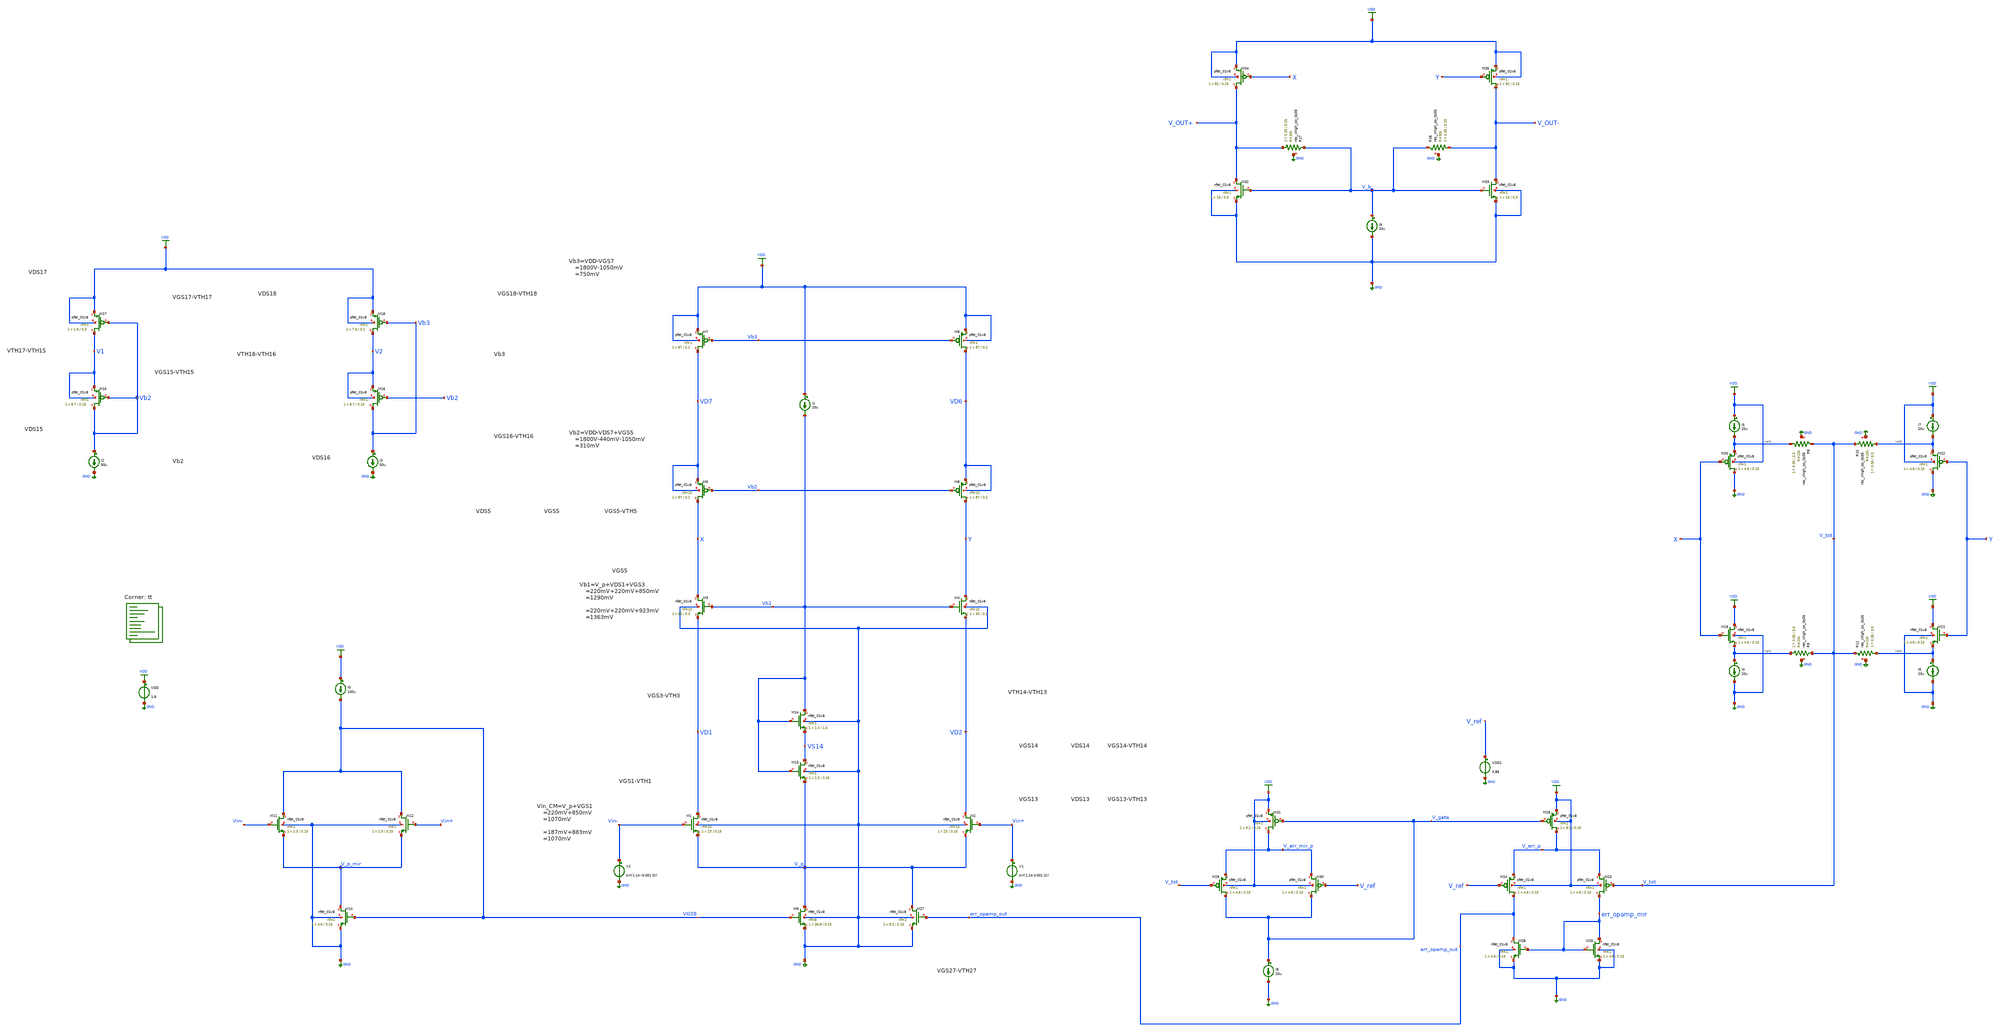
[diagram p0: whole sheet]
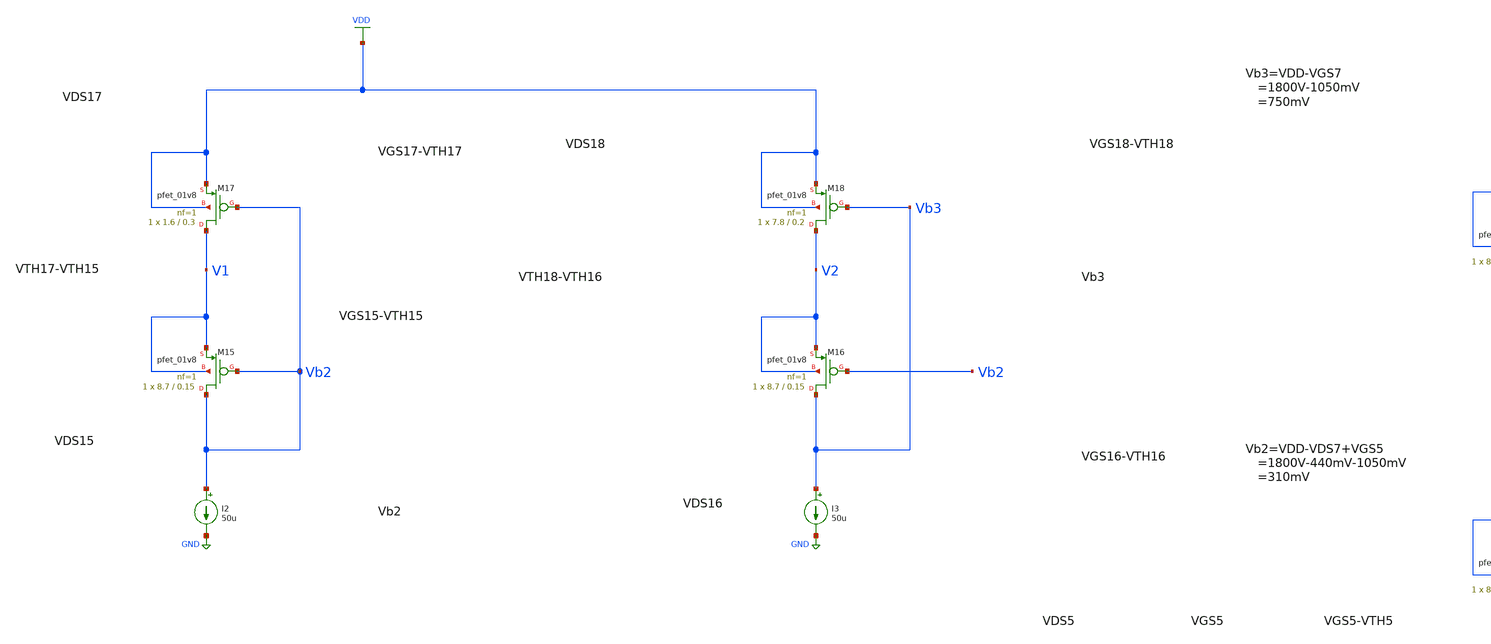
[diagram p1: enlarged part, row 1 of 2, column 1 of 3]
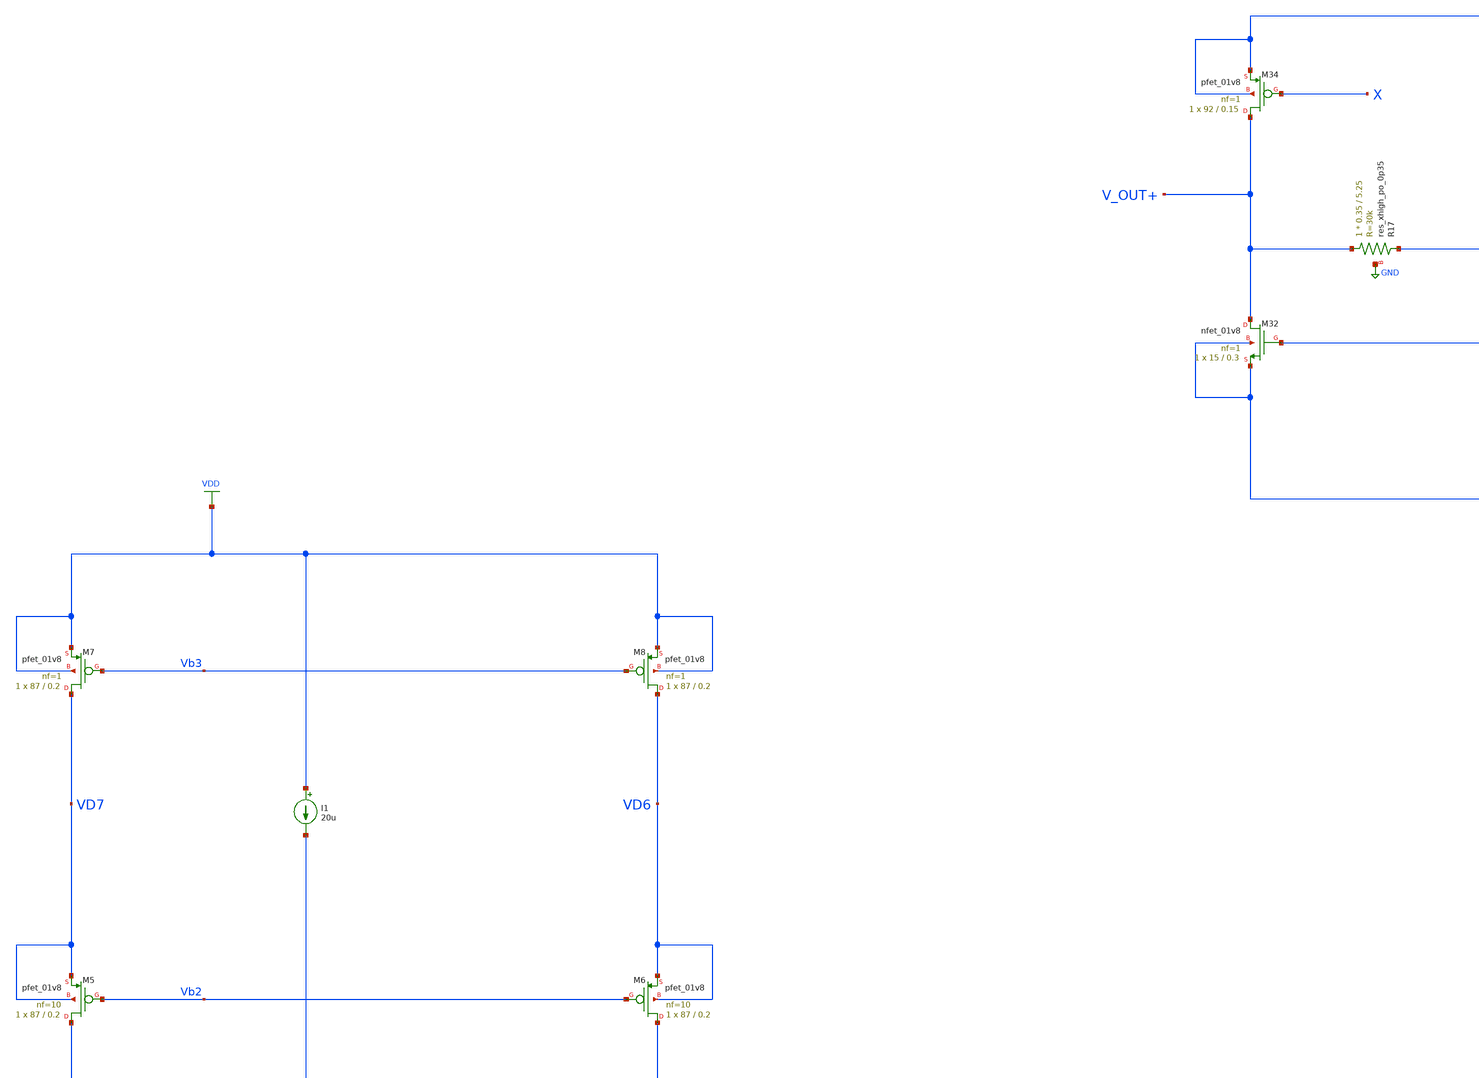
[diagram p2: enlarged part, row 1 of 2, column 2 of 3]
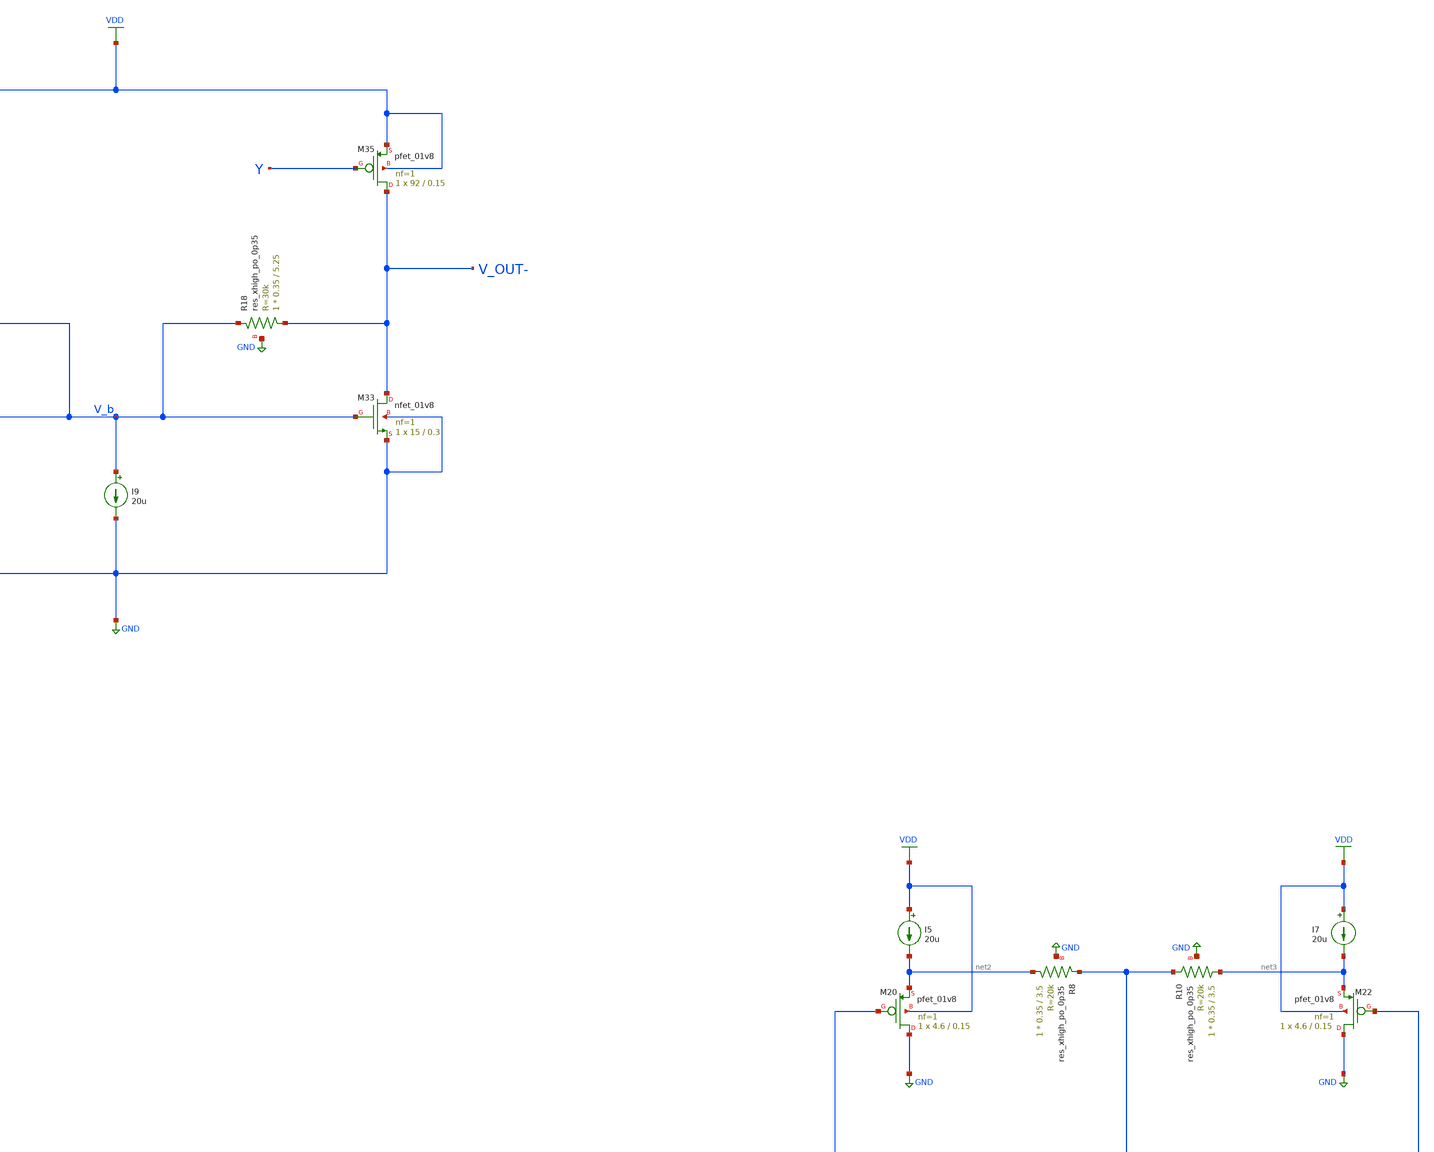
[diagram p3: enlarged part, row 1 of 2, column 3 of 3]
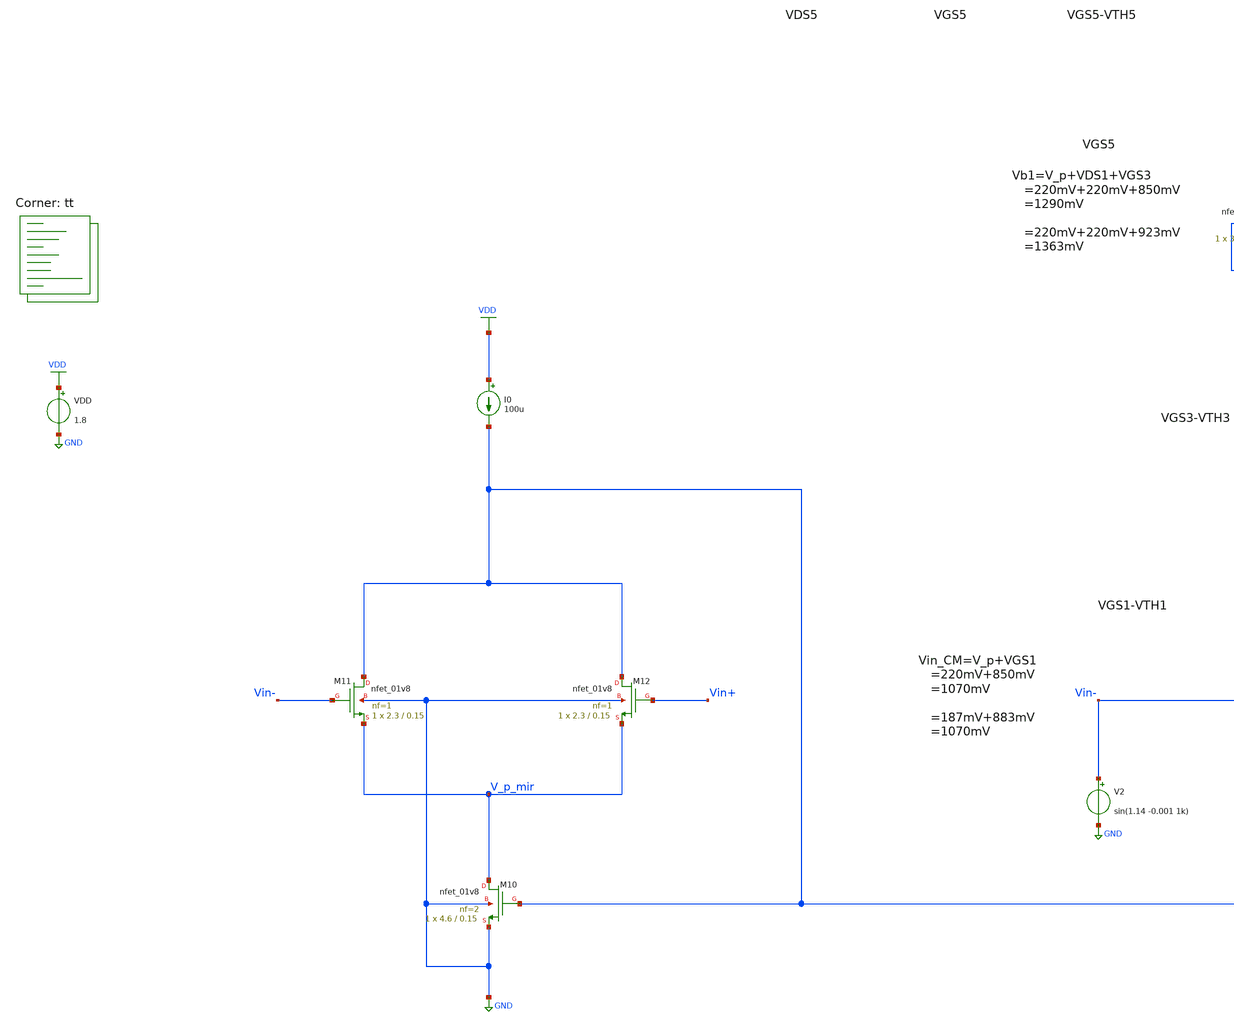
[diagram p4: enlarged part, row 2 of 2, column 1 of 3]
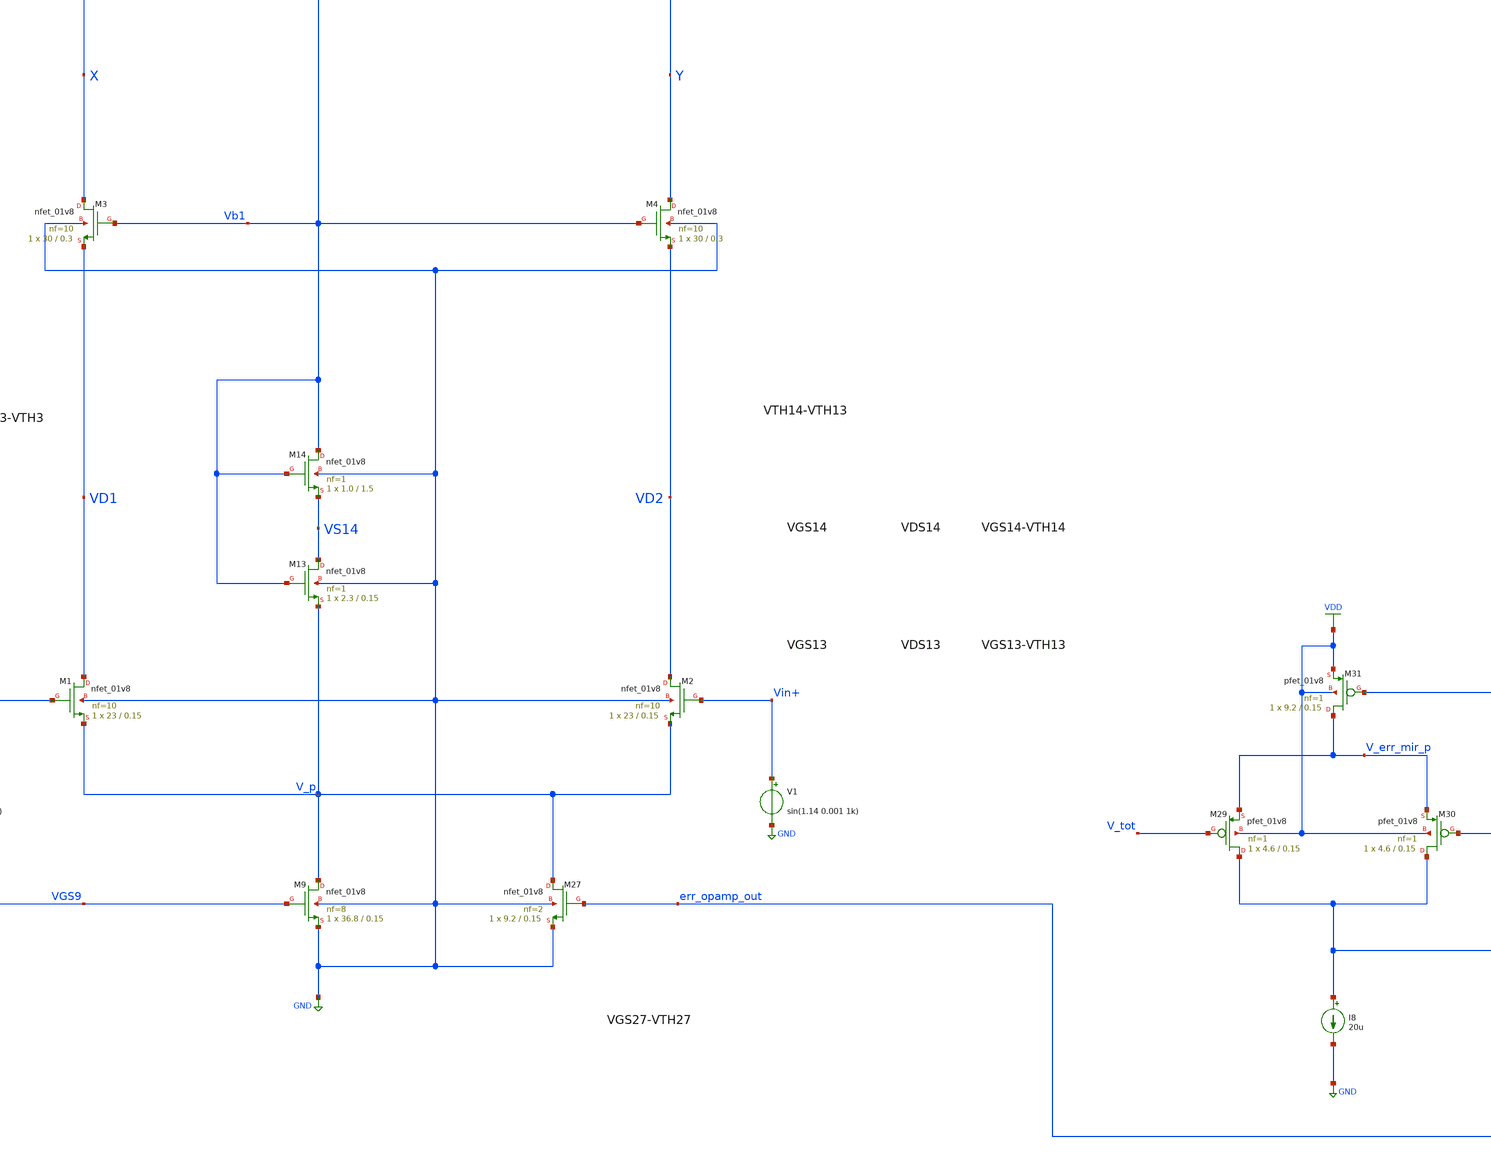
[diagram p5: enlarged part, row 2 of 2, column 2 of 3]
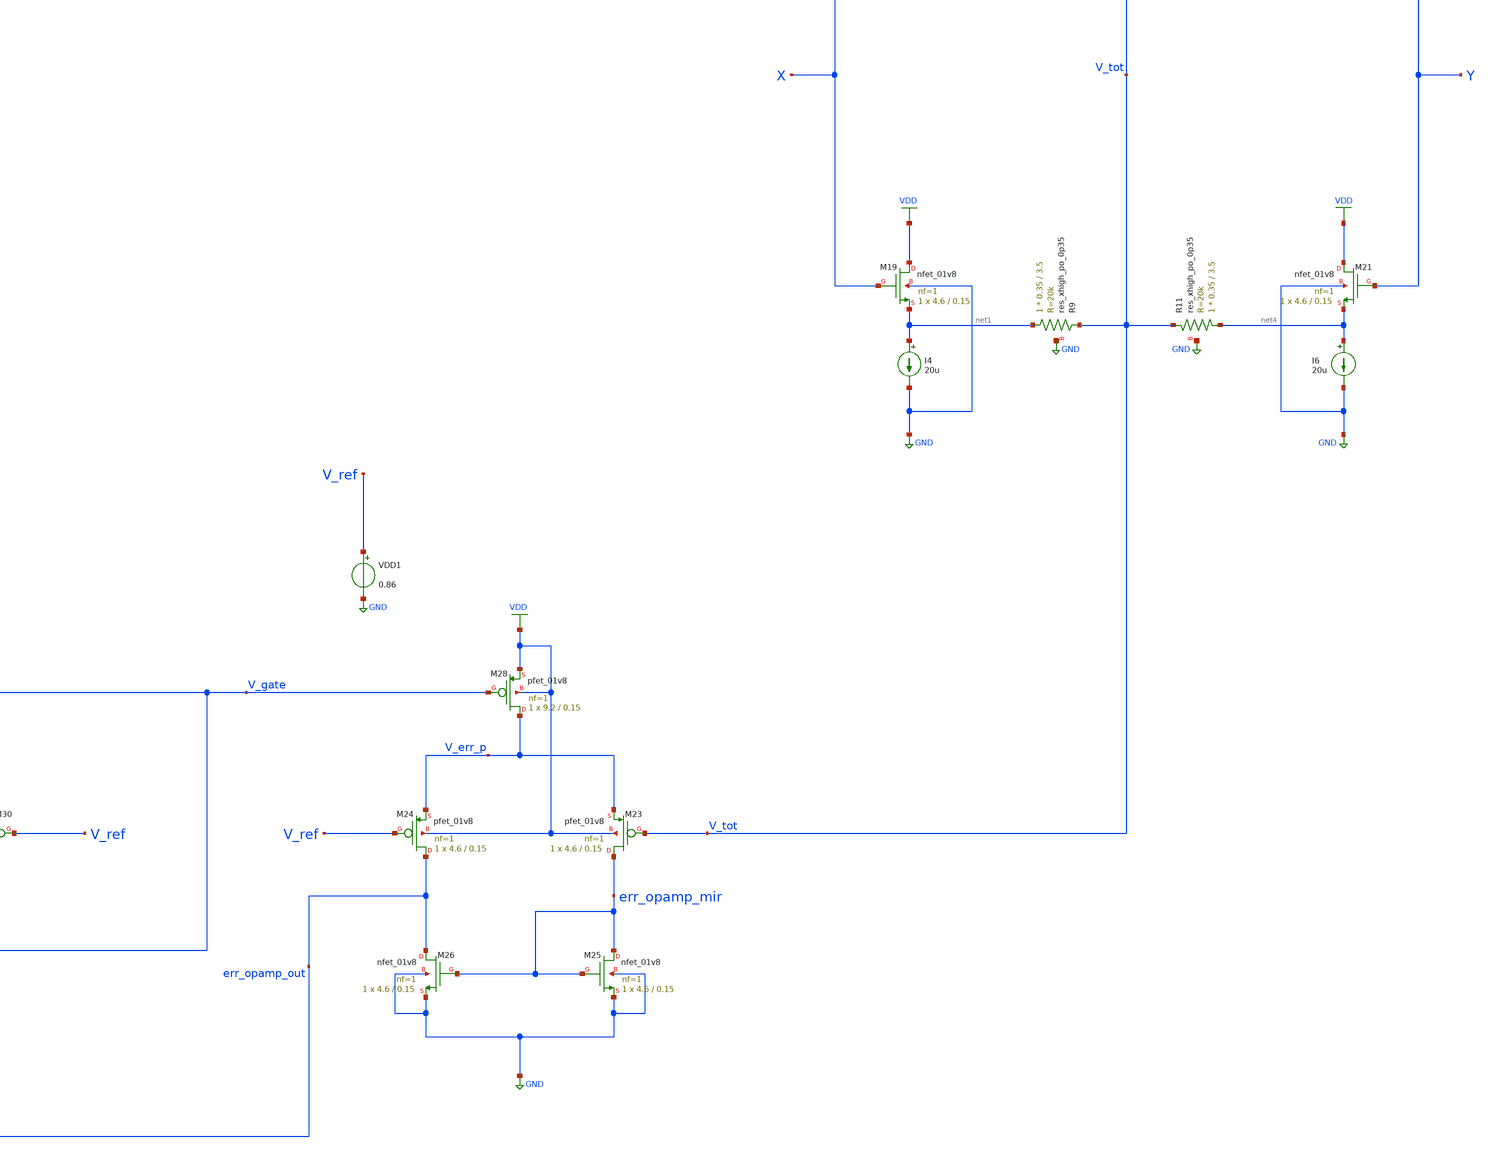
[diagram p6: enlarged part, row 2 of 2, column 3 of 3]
** sch_path: projects/opamp/xschem_ngspice/opamp_1st_stage_bias_check.sch
**.subckt opamp_1st_stage_bias_check
VDD VDD GND 1.8
XM1 VD1 Vin- V_p GND sky130_fd_pr__nfet_01v8 L=0.15 W=23 nf=10 ad='int((nf+1)/2) * W/nf * 0.29' as='int((nf+2)/2) * W/nf * 0.29'
+ pd='2*int((nf+1)/2) * (W/nf + 0.29)' ps='2*int((nf+2)/2) * (W/nf + 0.29)' nrd='0.29 / W' nrs='0.29 / W'
+ sa=0 sb=0 sd=0 mult=1 m=1
XM2 VD2 Vin+ V_p GND sky130_fd_pr__nfet_01v8 L=0.15 W=23 nf=10 ad='int((nf+1)/2) * W/nf * 0.29' as='int((nf+2)/2) * W/nf * 0.29'
+ pd='2*int((nf+1)/2) * (W/nf + 0.29)' ps='2*int((nf+2)/2) * (W/nf + 0.29)' nrd='0.29 / W' nrs='0.29 / W'
+ sa=0 sb=0 sd=0 mult=1 m=1
XM3 X Vb1 VD1 GND sky130_fd_pr__nfet_01v8 L=0.3 W=30 nf=10 ad='int((nf+1)/2) * W/nf * 0.29' as='int((nf+2)/2) * W/nf * 0.29'
+ pd='2*int((nf+1)/2) * (W/nf + 0.29)' ps='2*int((nf+2)/2) * (W/nf + 0.29)' nrd='0.29 / W' nrs='0.29 / W'
+ sa=0 sb=0 sd=0 mult=1 m=1
XM4 Y Vb1 VD2 GND sky130_fd_pr__nfet_01v8 L=0.3 W=30 nf=10 ad='int((nf+1)/2) * W/nf * 0.29' as='int((nf+2)/2) * W/nf * 0.29'
+ pd='2*int((nf+1)/2) * (W/nf + 0.29)' ps='2*int((nf+2)/2) * (W/nf + 0.29)' nrd='0.29 / W' nrs='0.29 / W'
+ sa=0 sb=0 sd=0 mult=1 m=1
XM5 X Vb2 VD7 VD7 sky130_fd_pr__pfet_01v8 L=0.2 W=87 nf=10 ad='int((nf+1)/2) * W/nf * 0.29' as='int((nf+2)/2) * W/nf * 0.29'
+ pd='2*int((nf+1)/2) * (W/nf + 0.29)' ps='2*int((nf+2)/2) * (W/nf + 0.29)' nrd='0.29 / W' nrs='0.29 / W'
+ sa=0 sb=0 sd=0 mult=1 m=1
XM6 Y Vb2 VD6 VD6 sky130_fd_pr__pfet_01v8 L=0.2 W=87 nf=10 ad='int((nf+1)/2) * W/nf * 0.29' as='int((nf+2)/2) * W/nf * 0.29'
+ pd='2*int((nf+1)/2) * (W/nf + 0.29)' ps='2*int((nf+2)/2) * (W/nf + 0.29)' nrd='0.29 / W' nrs='0.29 / W'
+ sa=0 sb=0 sd=0 mult=1 m=1
XM7 VD7 Vb3 VDD VDD sky130_fd_pr__pfet_01v8 L=0.2 W=87 nf=1 ad='int((nf+1)/2) * W/nf * 0.29' as='int((nf+2)/2) * W/nf * 0.29'
+ pd='2*int((nf+1)/2) * (W/nf + 0.29)' ps='2*int((nf+2)/2) * (W/nf + 0.29)' nrd='0.29 / W' nrs='0.29 / W'
+ sa=0 sb=0 sd=0 mult=1 m=1
XM8 VD6 Vb3 VDD VDD sky130_fd_pr__pfet_01v8 L=0.2 W=87 nf=1 ad='int((nf+1)/2) * W/nf * 0.29' as='int((nf+2)/2) * W/nf * 0.29'
+ pd='2*int((nf+1)/2) * (W/nf + 0.29)' ps='2*int((nf+2)/2) * (W/nf + 0.29)' nrd='0.29 / W' nrs='0.29 / W'
+ sa=0 sb=0 sd=0 mult=1 m=1
XM9 V_p VGS9 GND GND sky130_fd_pr__nfet_01v8 L=0.15 W=36.8 nf=8 ad='int((nf+1)/2) * W/nf * 0.29' as='int((nf+2)/2) * W/nf * 0.29'
+ pd='2*int((nf+1)/2) * (W/nf + 0.29)' ps='2*int((nf+2)/2) * (W/nf + 0.29)' nrd='0.29 / W' nrs='0.29 / W'
+ sa=0 sb=0 sd=0 mult=1 m=1
V1 Vin+ GND sin(1.14 0.001 1k)
XM10 V_p_mir VGS9 GND GND sky130_fd_pr__nfet_01v8 L=0.15 W=4.6 nf=2 ad='int((nf+1)/2) * W/nf * 0.29'
+ as='int((nf+2)/2) * W/nf * 0.29' pd='2*int((nf+1)/2) * (W/nf + 0.29)' ps='2*int((nf+2)/2) * (W/nf + 0.29)'
+ nrd='0.29 / W' nrs='0.29 / W' sa=0 sb=0 sd=0 mult=1 m=1
I0 VDD VGS9 100u
XM11 VGS9 Vin- V_p_mir GND sky130_fd_pr__nfet_01v8 L=0.15 W=2.3 nf=1 ad='int((nf+1)/2) * W/nf * 0.29'
+ as='int((nf+2)/2) * W/nf * 0.29' pd='2*int((nf+1)/2) * (W/nf + 0.29)' ps='2*int((nf+2)/2) * (W/nf + 0.29)'
+ nrd='0.29 / W' nrs='0.29 / W' sa=0 sb=0 sd=0 mult=1 m=1
XM12 VGS9 Vin+ V_p_mir GND sky130_fd_pr__nfet_01v8 L=0.15 W=2.3 nf=1 ad='int((nf+1)/2) * W/nf * 0.29'
+ as='int((nf+2)/2) * W/nf * 0.29' pd='2*int((nf+1)/2) * (W/nf + 0.29)' ps='2*int((nf+2)/2) * (W/nf + 0.29)'
+ nrd='0.29 / W' nrs='0.29 / W' sa=0 sb=0 sd=0 mult=1 m=1
XM13 VS14 Vb1 V_p GND sky130_fd_pr__nfet_01v8 L=0.15 W=2.3 nf=1 ad='int((nf+1)/2) * W/nf * 0.29' as='int((nf+2)/2) * W/nf * 0.29'
+ pd='2*int((nf+1)/2) * (W/nf + 0.29)' ps='2*int((nf+2)/2) * (W/nf + 0.29)' nrd='0.29 / W' nrs='0.29 / W'
+ sa=0 sb=0 sd=0 mult=1 m=1
XM14 Vb1 Vb1 VS14 GND sky130_fd_pr__nfet_01v8 L=1.5 W=1.0 nf=1 ad='int((nf+1)/2) * W/nf * 0.29' as='int((nf+2)/2) * W/nf * 0.29'
+ pd='2*int((nf+1)/2) * (W/nf + 0.29)' ps='2*int((nf+2)/2) * (W/nf + 0.29)' nrd='0.29 / W' nrs='0.29 / W'
+ sa=0 sb=0 sd=0 mult=1 m=1
I1 VDD Vb1 20u
XM15 Vb2 Vb2 V1 V1 sky130_fd_pr__pfet_01v8 L=0.15 W=8.7 nf=1 ad='int((nf+1)/2) * W/nf * 0.29' as='int((nf+2)/2) * W/nf * 0.29'
+ pd='2*int((nf+1)/2) * (W/nf + 0.29)' ps='2*int((nf+2)/2) * (W/nf + 0.29)' nrd='0.29 / W' nrs='0.29 / W'
+ sa=0 sb=0 sd=0 mult=1 m=1
XM16 Vb3 Vb2 V2 V2 sky130_fd_pr__pfet_01v8 L=0.15 W=8.7 nf=1 ad='int((nf+1)/2) * W/nf * 0.29' as='int((nf+2)/2) * W/nf * 0.29'
+ pd='2*int((nf+1)/2) * (W/nf + 0.29)' ps='2*int((nf+2)/2) * (W/nf + 0.29)' nrd='0.29 / W' nrs='0.29 / W'
+ sa=0 sb=0 sd=0 mult=1 m=1
XM17 V1 Vb2 VDD VDD sky130_fd_pr__pfet_01v8 L=0.3 W=1.6 nf=1 ad='int((nf+1)/2) * W/nf * 0.29' as='int((nf+2)/2) * W/nf * 0.29'
+ pd='2*int((nf+1)/2) * (W/nf + 0.29)' ps='2*int((nf+2)/2) * (W/nf + 0.29)' nrd='0.29 / W' nrs='0.29 / W'
+ sa=0 sb=0 sd=0 mult=1 m=1
XM18 V2 Vb3 VDD VDD sky130_fd_pr__pfet_01v8 L=0.2 W=7.8 nf=1 ad='int((nf+1)/2) * W/nf * 0.29' as='int((nf+2)/2) * W/nf * 0.29'
+ pd='2*int((nf+1)/2) * (W/nf + 0.29)' ps='2*int((nf+2)/2) * (W/nf + 0.29)' nrd='0.29 / W' nrs='0.29 / W'
+ sa=0 sb=0 sd=0 mult=1 m=1
I2 Vb2 GND 50u
I3 Vb3 GND 50u
XM19 VDD X net1 GND sky130_fd_pr__nfet_01v8 L=0.15 W=4.6 nf=1 ad='int((nf+1)/2) * W/nf * 0.29' as='int((nf+2)/2) * W/nf * 0.29'
+ pd='2*int((nf+1)/2) * (W/nf + 0.29)' ps='2*int((nf+2)/2) * (W/nf + 0.29)' nrd='0.29 / W' nrs='0.29 / W'
+ sa=0 sb=0 sd=0 mult=1 m=1
XM20 GND X net2 VDD sky130_fd_pr__pfet_01v8 L=0.15 W=4.6 nf=1 ad='int((nf+1)/2) * W/nf * 0.29' as='int((nf+2)/2) * W/nf * 0.29'
+ pd='2*int((nf+1)/2) * (W/nf + 0.29)' ps='2*int((nf+2)/2) * (W/nf + 0.29)' nrd='0.29 / W' nrs='0.29 / W'
+ sa=0 sb=0 sd=0 mult=1 m=1
I4 net1 GND 20u
I5 VDD net2 20u
XR8 net2 V_tot GND sky130_fd_pr__res_xhigh_po_0p35 L=3.5 mult=1 m=1
XR9 net1 V_tot GND sky130_fd_pr__res_xhigh_po_0p35 L=3.5 mult=1 m=1
XR10 net3 V_tot GND sky130_fd_pr__res_xhigh_po_0p35 L=3.5 mult=1 m=1
XR11 net4 V_tot GND sky130_fd_pr__res_xhigh_po_0p35 L=3.5 mult=1 m=1
XM21 VDD Y net4 GND sky130_fd_pr__nfet_01v8 L=0.15 W=4.6 nf=1 ad='int((nf+1)/2) * W/nf * 0.29' as='int((nf+2)/2) * W/nf * 0.29'
+ pd='2*int((nf+1)/2) * (W/nf + 0.29)' ps='2*int((nf+2)/2) * (W/nf + 0.29)' nrd='0.29 / W' nrs='0.29 / W'
+ sa=0 sb=0 sd=0 mult=1 m=1
XM22 GND Y net3 VDD sky130_fd_pr__pfet_01v8 L=0.15 W=4.6 nf=1 ad='int((nf+1)/2) * W/nf * 0.29' as='int((nf+2)/2) * W/nf * 0.29'
+ pd='2*int((nf+1)/2) * (W/nf + 0.29)' ps='2*int((nf+2)/2) * (W/nf + 0.29)' nrd='0.29 / W' nrs='0.29 / W'
+ sa=0 sb=0 sd=0 mult=1 m=1
I6 net4 GND 20u
I7 VDD net3 20u
XM23 err_opamp_mir V_tot V_err_p VDD sky130_fd_pr__pfet_01v8 L=0.15 W=4.6 nf=1 ad='int((nf+1)/2) * W/nf * 0.29'
+ as='int((nf+2)/2) * W/nf * 0.29' pd='2*int((nf+1)/2) * (W/nf + 0.29)' ps='2*int((nf+2)/2) * (W/nf + 0.29)'
+ nrd='0.29 / W' nrs='0.29 / W' sa=0 sb=0 sd=0 mult=1 m=1
XM24 err_opamp_out V_ref V_err_p VDD sky130_fd_pr__pfet_01v8 L=0.15 W=4.6 nf=1 ad='int((nf+1)/2) * W/nf * 0.29'
+ as='int((nf+2)/2) * W/nf * 0.29' pd='2*int((nf+1)/2) * (W/nf + 0.29)' ps='2*int((nf+2)/2) * (W/nf + 0.29)'
+ nrd='0.29 / W' nrs='0.29 / W' sa=0 sb=0 sd=0 mult=1 m=1
I8 V_gate GND 20u
XM25 err_opamp_mir err_opamp_mir GND GND sky130_fd_pr__nfet_01v8 L=0.15 W=4.6 nf=1 ad='int((nf+1)/2) * W/nf * 0.29'
+ as='int((nf+2)/2) * W/nf * 0.29' pd='2*int((nf+1)/2) * (W/nf + 0.29)' ps='2*int((nf+2)/2) * (W/nf + 0.29)'
+ nrd='0.29 / W' nrs='0.29 / W' sa=0 sb=0 sd=0 mult=1 m=1
XM26 err_opamp_out err_opamp_mir GND GND sky130_fd_pr__nfet_01v8 L=0.15 W=4.6 nf=1 ad='int((nf+1)/2) * W/nf * 0.29'
+ as='int((nf+2)/2) * W/nf * 0.29' pd='2*int((nf+1)/2) * (W/nf + 0.29)' ps='2*int((nf+2)/2) * (W/nf + 0.29)'
+ nrd='0.29 / W' nrs='0.29 / W' sa=0 sb=0 sd=0 mult=1 m=1
XM27 V_p err_opamp_out GND GND sky130_fd_pr__nfet_01v8 L=0.15 W=9.2 nf=2 ad='int((nf+1)/2) * W/nf * 0.29'
+ as='int((nf+2)/2) * W/nf * 0.29' pd='2*int((nf+1)/2) * (W/nf + 0.29)' ps='2*int((nf+2)/2) * (W/nf + 0.29)'
+ nrd='0.29 / W' nrs='0.29 / W' sa=0 sb=0 sd=0 mult=1 m=1
VDD1 V_ref GND 0.86
XM28 V_err_p V_gate VDD VDD sky130_fd_pr__pfet_01v8 L=0.15 W=9.2 nf=1 ad='int((nf+1)/2) * W/nf * 0.29'
+ as='int((nf+2)/2) * W/nf * 0.29' pd='2*int((nf+1)/2) * (W/nf + 0.29)' ps='2*int((nf+2)/2) * (W/nf + 0.29)'
+ nrd='0.29 / W' nrs='0.29 / W' sa=0 sb=0 sd=0 mult=1 m=1
XM29 V_gate V_tot V_err_mir_p VDD sky130_fd_pr__pfet_01v8 L=0.15 W=4.6 nf=1 ad='int((nf+1)/2) * W/nf * 0.29'
+ as='int((nf+2)/2) * W/nf * 0.29' pd='2*int((nf+1)/2) * (W/nf + 0.29)' ps='2*int((nf+2)/2) * (W/nf + 0.29)'
+ nrd='0.29 / W' nrs='0.29 / W' sa=0 sb=0 sd=0 mult=1 m=1
XM30 V_gate V_ref V_err_mir_p VDD sky130_fd_pr__pfet_01v8 L=0.15 W=4.6 nf=1 ad='int((nf+1)/2) * W/nf * 0.29'
+ as='int((nf+2)/2) * W/nf * 0.29' pd='2*int((nf+1)/2) * (W/nf + 0.29)' ps='2*int((nf+2)/2) * (W/nf + 0.29)'
+ nrd='0.29 / W' nrs='0.29 / W' sa=0 sb=0 sd=0 mult=1 m=1
XM31 V_err_mir_p V_gate VDD VDD sky130_fd_pr__pfet_01v8 L=0.15 W=9.2 nf=1 ad='int((nf+1)/2) * W/nf * 0.29'
+ as='int((nf+2)/2) * W/nf * 0.29' pd='2*int((nf+1)/2) * (W/nf + 0.29)' ps='2*int((nf+2)/2) * (W/nf + 0.29)'
+ nrd='0.29 / W' nrs='0.29 / W' sa=0 sb=0 sd=0 mult=1 m=1
XM32 V_OUT+ V_b GND GND sky130_fd_pr__nfet_01v8 L=0.3 W=15 nf=1 ad='int((nf+1)/2) * W/nf * 0.29' as='int((nf+2)/2) * W/nf * 0.29'
+ pd='2*int((nf+1)/2) * (W/nf + 0.29)' ps='2*int((nf+2)/2) * (W/nf + 0.29)' nrd='0.29 / W' nrs='0.29 / W'
+ sa=0 sb=0 sd=0 mult=1 m=1
XM33 V_OUT- V_b GND GND sky130_fd_pr__nfet_01v8 L=0.3 W=15 nf=1 ad='int((nf+1)/2) * W/nf * 0.29' as='int((nf+2)/2) * W/nf * 0.29'
+ pd='2*int((nf+1)/2) * (W/nf + 0.29)' ps='2*int((nf+2)/2) * (W/nf + 0.29)' nrd='0.29 / W' nrs='0.29 / W'
+ sa=0 sb=0 sd=0 mult=1 m=1
XM34 V_OUT+ X VDD VDD sky130_fd_pr__pfet_01v8 L=0.15 W=92 nf=1 ad='int((nf+1)/2) * W/nf * 0.29' as='int((nf+2)/2) * W/nf * 0.29'
+ pd='2*int((nf+1)/2) * (W/nf + 0.29)' ps='2*int((nf+2)/2) * (W/nf + 0.29)' nrd='0.29 / W' nrs='0.29 / W'
+ sa=0 sb=0 sd=0 mult=1 m=1
XM35 V_OUT- Y VDD VDD sky130_fd_pr__pfet_01v8 L=0.15 W=92 nf=1 ad='int((nf+1)/2) * W/nf * 0.29' as='int((nf+2)/2) * W/nf * 0.29'
+ pd='2*int((nf+1)/2) * (W/nf + 0.29)' ps='2*int((nf+2)/2) * (W/nf + 0.29)' nrd='0.29 / W' nrs='0.29 / W'
+ sa=0 sb=0 sd=0 mult=1 m=1
XR17 V_OUT+ V_b GND sky130_fd_pr__res_xhigh_po_0p35 L=5.25 mult=1 m=1
XR18 V_OUT- V_b GND sky130_fd_pr__res_xhigh_po_0p35 L=5.25 mult=1 m=1
I9 V_b GND 20u
V2 Vin- GND sin(1.14 -0.001 1k)
**** begin user architecture code



.option method=gear
.option wnflag=1
.option savecurrents

.save @m.xm1.msky130_fd_pr__nfet_01v8[gm] @m.xm1.msky130_fd_pr__nfet_01v8[vth] @m.xm2.msky130_fd_pr__nfet_01v8[gm] @m.xm2.msky130_fd_pr__nfet_01v8[vth] @m.xm3.msky130_fd_pr__nfet_01v8[gm] @m.xm3.msky130_fd_pr__nfet_01v8[vth] @m.xm4.msky130_fd_pr__nfet_01v8[gm] @m.xm4.msky130_fd_pr__nfet_01v8[vth] @m.xm5.msky130_fd_pr__pfet_01v8[gm] @m.xm5.msky130_fd_pr__pfet_01v8[vth] @m.xm6.msky130_fd_pr__pfet_01v8[gm] @m.xm6.msky130_fd_pr__pfet_01v8[vth] @m.xm7.msky130_fd_pr__pfet_01v8[gm] @m.xm7.msky130_fd_pr__pfet_01v8[vth] @m.xm8.msky130_fd_pr__pfet_01v8[gm] @m.xm8.msky130_fd_pr__pfet_01v8[vth] @m.xm9.msky130_fd_pr__nfet_01v8[gm] @m.xm9.msky130_fd_pr__nfet_01v8[vth] @m.xm10.msky130_fd_pr__nfet_01v8[gm] @m.xm10.msky130_fd_pr__nfet_01v8[vth] @m.xm11.msky130_fd_pr__nfet_01v8[gm] @m.xm11.msky130_fd_pr__nfet_01v8[vth] @m.xm12.msky130_fd_pr__nfet_01v8[gm] @m.xm12.msky130_fd_pr__nfet_01v8[vth] @m.xm13.msky130_fd_pr__nfet_01v8[gm] @m.xm13.msky130_fd_pr__nfet_01v8[vth] @m.xm14.msky130_fd_pr__nfet_01v8[gm] @m.xm14.msky130_fd_pr__nfet_01v8[vth] @m.xm15.msky130_fd_pr__pfet_01v8[gm] @m.xm15.msky130_fd_pr__pfet_01v8[vth] @m.xm16.msky130_fd_pr__pfet_01v8[gm] @m.xm16.msky130_fd_pr__pfet_01v8[vth] @m.xm17.msky130_fd_pr__pfet_01v8[gm] @m.xm17.msky130_fd_pr__pfet_01v8[vth] @m.xm18.msky130_fd_pr__pfet_01v8[gm] @m.xm18.msky130_fd_pr__pfet_01v8[vth] @m.xm19.msky130_fd_pr__nfet_01v8[gm] @m.xm19.msky130_fd_pr__nfet_01v8[vth] @m.xm20.msky130_fd_pr__pfet_01v8[gm] @m.xm20.msky130_fd_pr__pfet_01v8[vth] @m.xm21.msky130_fd_pr__nfet_01v8[gm] @m.xm21.msky130_fd_pr__nfet_01v8[vth] @m.xm22.msky130_fd_pr__pfet_01v8[gm] @m.xm22.msky130_fd_pr__pfet_01v8[vth] @m.xm23.msky130_fd_pr__pfet_01v8[gm] @m.xm23.msky130_fd_pr__pfet_01v8[vth] @m.xm24.msky130_fd_pr__pfet_01v8[gm] @m.xm24.msky130_fd_pr__pfet_01v8[vth] @m.xm25.msky130_fd_pr__nfet_01v8[gm] @m.xm25.msky130_fd_pr__nfet_01v8[vth] @m.xm26.msky130_fd_pr__nfet_01v8[gm] @m.xm26.msky130_fd_pr__nfet_01v8[vth] @m.xm27.msky130_fd_pr__nfet_01v8[gm] @m.xm27.msky130_fd_pr__nfet_01v8[vth] @m.xm28.msky130_fd_pr__nfet_01v8[gm] @m.xm28.msky130_fd_pr__nfet_01v8[vth] @m.xm29.msky130_fd_pr__nfet_01v8[gm] @m.xm29.msky130_fd_pr__nfet_01v8[vth] @m.xm30.msky130_fd_pr__nfet_01v8[gm] @m.xm30.msky130_fd_pr__nfet_01v8[vth] @m.xm31.msky130_fd_pr__nfet_01v8[gm] @m.xm31.msky130_fd_pr__nfet_01v8[vth] @m.xm32.msky130_fd_pr__nfet_01v8[gm] @m.xm32.msky130_fd_pr__nfet_01v8[vth] @m.xm33.msky130_fd_pr__nfet_01v8[gm] @m.xm33.msky130_fd_pr__nfet_01v8[vth] @m.xm34.msky130_fd_pr__pfet_01v8[gm] @m.xm34.msky130_fd_pr__pfet_01v8[vth] @m.xm35.msky130_fd_pr__pfet_01v8[gm] @m.xm35.msky130_fd_pr__pfet_01v8[vth]


.control

  save all
  * dc VDD 0 1.8 0.9
  * ac dec 20 1 1T
  tran 1ns 12us
  remzerovec
  write opamp_1st_stage_bias_check.raw
  set appendwrite

.endc




.lib $::SKYWATER_MODELS/sky130.lib.spice tt
**** end user architecture code
**.ends
.GLOBAL GND
.GLOBAL VDD
.end
